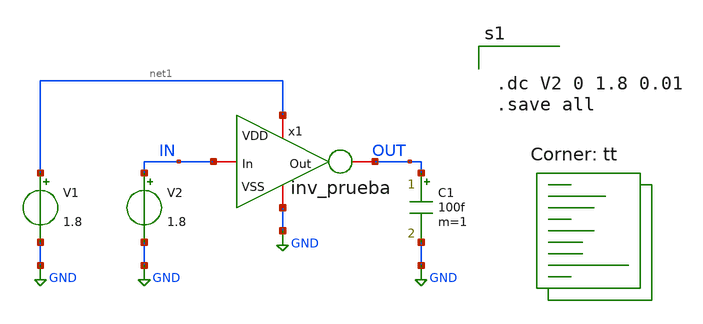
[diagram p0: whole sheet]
** sch_path: HVT/xschem_pruebas/tb_inv_sweep.sch
**.subckt tb_inv_sweep
x1 net1 OUT IN GND inv_prueba
V2 IN GND 1.8
V1 net1 GND 1.8
C1 OUT GND 100f m=1
**** begin user architecture code


.dc V2 0 1.8 0.01
.save all


.lib $::SKYWATER_MODELS/sky130.lib.spice tt
**** end user architecture code
**.ends

* expanding   symbol:  /foss/designs/xschem_pruebas/inv_prueba.sym # of pins=4
** sym_path: HVT/xschem_pruebas/inv_prueba.sym
** sch_path: HVT/xschem_pruebas/inv_prueba.sch
.subckt inv_prueba VDD Out In VSS
*.iopin Out
*.iopin In
*.iopin VDD
*.iopin VSS
XM3 Out In VDD VDD sky130_fd_pr__pfet_01v8 L=0.15 W=1 nf=1 ad='int((nf+1)/2) * W/nf * 0.29' as='int((nf+2)/2) * W/nf * 0.29'
+ pd='2*int((nf+1)/2) * (W/nf + 0.29)' ps='2*int((nf+2)/2) * (W/nf + 0.29)' nrd='0.29 / W' nrs='0.29 / W'
+ sa=0 sb=0 sd=0 mult=1 m=1
XM4 Out In VSS VSS sky130_fd_pr__nfet_01v8 L=0.15 W=1 nf=1 ad='int((nf+1)/2) * W/nf * 0.29' as='int((nf+2)/2) * W/nf * 0.29'
+ pd='2*int((nf+1)/2) * (W/nf + 0.29)' ps='2*int((nf+2)/2) * (W/nf + 0.29)' nrd='0.29 / W' nrs='0.29 / W'
+ sa=0 sb=0 sd=0 mult=1 m=1
.ends

.GLOBAL GND
.end
